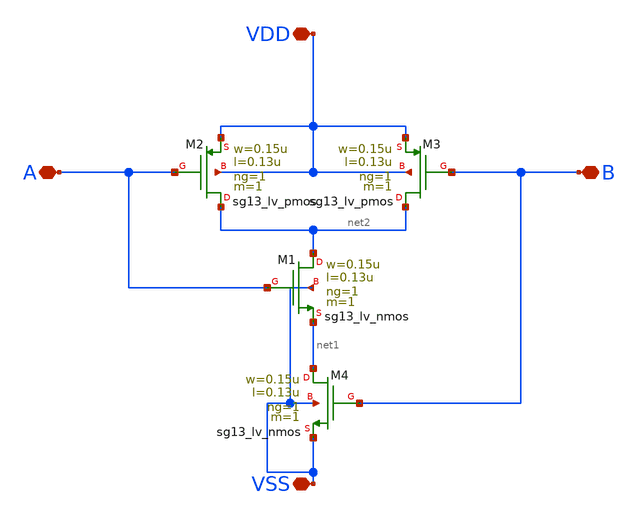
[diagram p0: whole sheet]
** sch_path: blocks/nand/nand.sch
**.subckt nand VDD VSS A B
*.iopin VDD
*.iopin VSS
*.iopin A
*.iopin B
XM1 net2 A net1 VSS sg13_lv_nmos w=0.15u l=0.13u ng=1 m=1 mm_ok=1
XM2 net2 A VDD VDD sg13_lv_pmos w=0.15u l=0.13u ng=1 m=1 mm_ok=1
XM3 net2 B VDD VDD sg13_lv_pmos w=0.15u l=0.13u ng=1 m=1 mm_ok=1
XM4 net1 B VSS VSS sg13_lv_nmos w=0.15u l=0.13u ng=1 m=1 mm_ok=1
**.ends
.end
